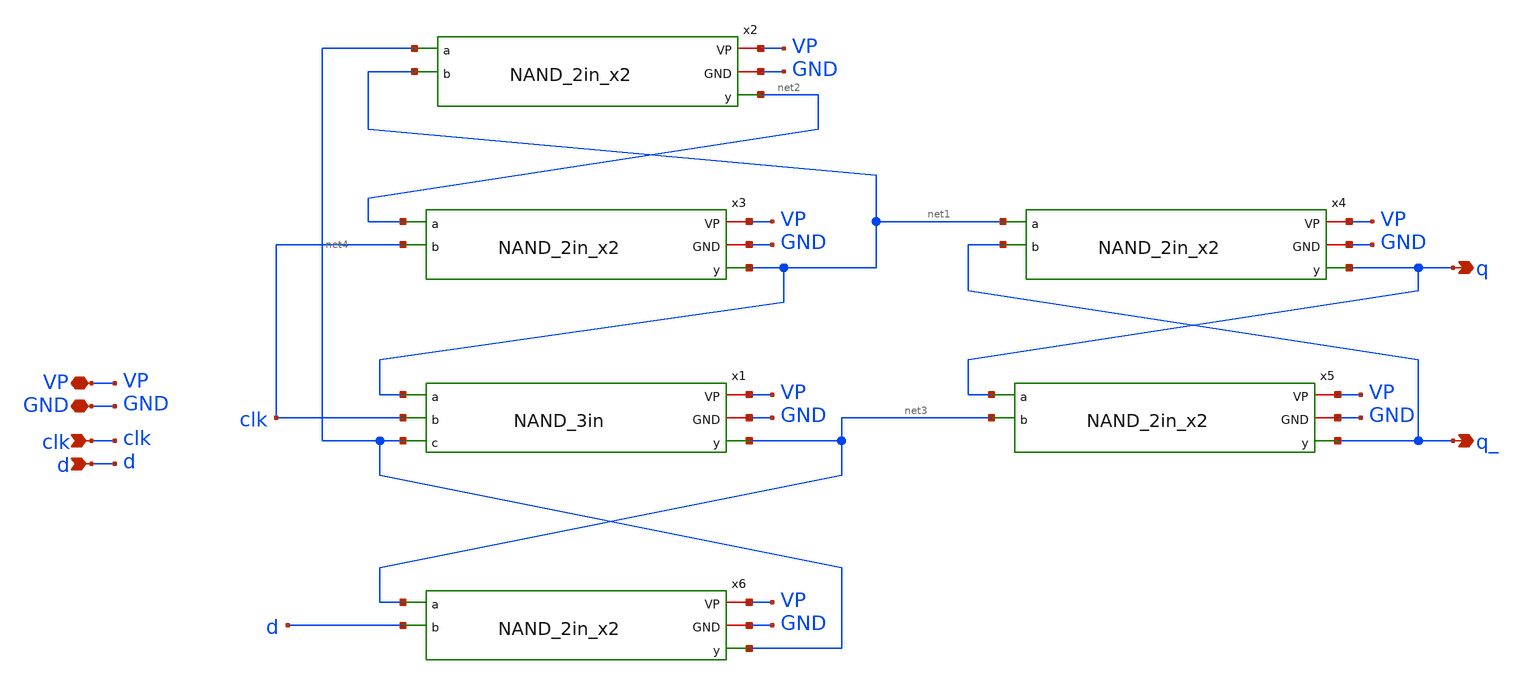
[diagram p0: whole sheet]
** sch_path: PLL0663-main/schematic/xschem/divider/d_flip_flop.sch
**.subckt d_flip_flop GND clk VP d q q_
*.iopin GND
*.ipin clk
*.iopin VP
*.ipin d
*.opin q
*.opin q_
x1 VP GND net1 net3 clk net4 NAND_3in
x2 VP GND net4 net2 net1 NAND_2in_x2
x3 VP GND net2 net1 clk NAND_2in_x2
x4 VP GND net1 q q_ NAND_2in_x2
x5 VP GND q q_ net3 NAND_2in_x2
x6 VP GND net3 net4 d NAND_2in_x2
**.ends
.end
